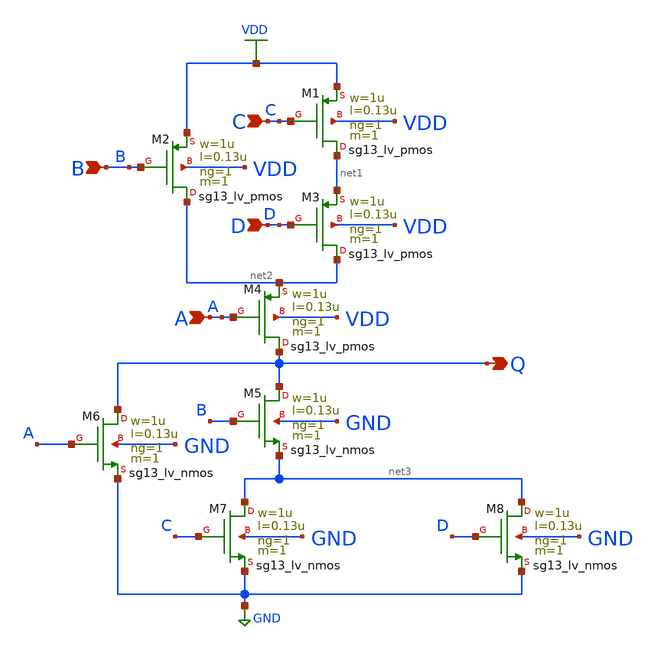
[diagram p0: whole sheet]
** sch_path: Modulo_Digital/Lab1/cmos_funct2.sch
**.subckt cmos_funct2 Q B C D A
*.opin Q
*.ipin B
*.ipin C
*.ipin D
*.ipin A
XM1 net1 C VDD VDD sg13_lv_pmos w=1u l=0.13u ng=1 m=1 mm_ok=1
XM2 net2 B VDD VDD sg13_lv_pmos w=1u l=0.13u ng=1 m=1 mm_ok=1
XM3 net2 D net1 VDD sg13_lv_pmos w=1u l=0.13u ng=1 m=1 mm_ok=1
XM4 Q A net2 VDD sg13_lv_pmos w=1u l=0.13u ng=1 m=1 mm_ok=1
XM5 Q B net3 GND sg13_lv_nmos w=1u l=0.13u ng=1 m=1 mm_ok=1
XM6 Q A GND GND sg13_lv_nmos w=1u l=0.13u ng=1 m=1 mm_ok=1
XM7 net3 C GND GND sg13_lv_nmos w=1u l=0.13u ng=1 m=1 mm_ok=1
XM8 net3 D GND GND sg13_lv_nmos w=1u l=0.13u ng=1 m=1 mm_ok=1
**.ends
.GLOBAL GND
.GLOBAL VDD
.end
